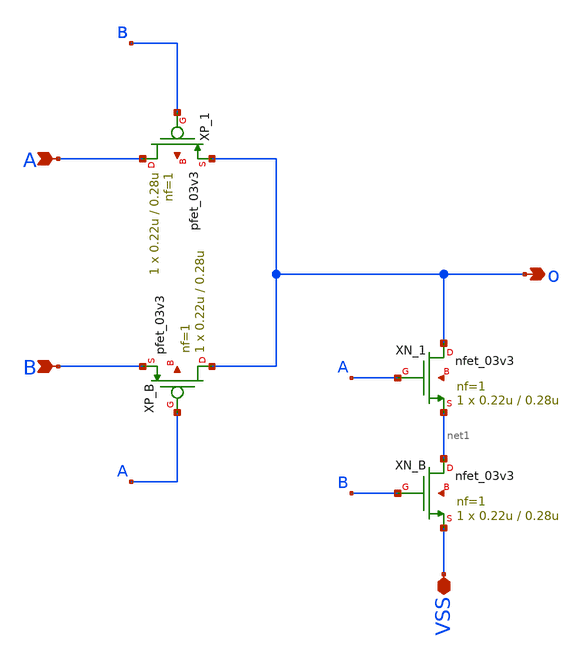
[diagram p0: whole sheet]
** sch_path: schematics/pass4_xor.sch
**.subckt pass4_xor VSS o A B
*.iopin VSS
*.opin o
*.ipin A
*.ipin B
XP_B o A B net2 pfet_03v3 L=0.28u W=0.22u nf=1 ad='int((nf+1)/2) * W/nf * 0.18u' as='int((nf+2)/2) * W/nf * 0.18u'
+ pd='2*int((nf+1)/2) * (W/nf + 0.18u)' ps='2*int((nf+2)/2) * (W/nf + 0.18u)' nrd='0.18u / W' nrs='0.18u / W'
+ sa=0 sb=0 sd=0 m=1
XN_B net1 B VSS net3 nfet_03v3 L=0.28u W=0.22u nf=1 ad='int((nf+1)/2) * W/nf * 0.18u' as='int((nf+2)/2) * W/nf * 0.18u'
+ pd='2*int((nf+1)/2) * (W/nf + 0.18u)' ps='2*int((nf+2)/2) * (W/nf + 0.18u)' nrd='0.18u / W' nrs='0.18u / W'
+ sa=0 sb=0 sd=0 m=1
XP_1 A B o net4 pfet_03v3 L=0.28u W=0.22u nf=1 ad='int((nf+1)/2) * W/nf * 0.18u' as='int((nf+2)/2) * W/nf * 0.18u'
+ pd='2*int((nf+1)/2) * (W/nf + 0.18u)' ps='2*int((nf+2)/2) * (W/nf + 0.18u)' nrd='0.18u / W' nrs='0.18u / W'
+ sa=0 sb=0 sd=0 m=1
XN_1 o A net1 net5 nfet_03v3 L=0.28u W=0.22u nf=1 ad='int((nf+1)/2) * W/nf * 0.18u' as='int((nf+2)/2) * W/nf * 0.18u'
+ pd='2*int((nf+1)/2) * (W/nf + 0.18u)' ps='2*int((nf+2)/2) * (W/nf + 0.18u)' nrd='0.18u / W' nrs='0.18u / W'
+ sa=0 sb=0 sd=0 m=1
**.ends
.end
